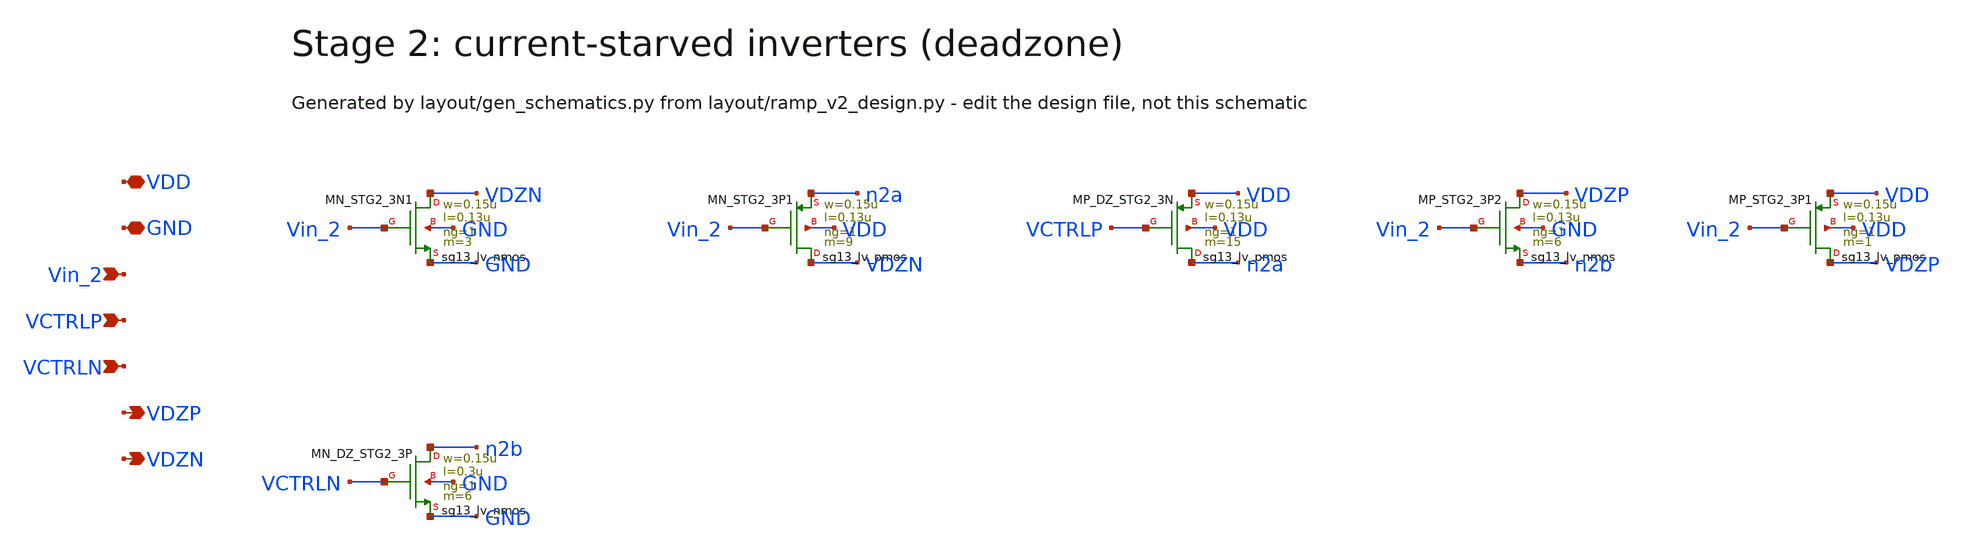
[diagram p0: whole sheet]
** sch_path: Design Files/RAMP/RAMP-V2/STG2_V2.sch
**.subckt STG2_V2 VDD GND Vin_2 VCTRLP VCTRLN VDZP VDZN
*.iopin VDD
*.iopin GND
*.ipin Vin_2
*.ipin VCTRLP
*.ipin VCTRLN
*.opin VDZP
*.opin VDZN
XMN_STG2_3N1 VDZN Vin_2 GND GND sg13_lv_nmos w=0.15u l=0.13u ng=1 m=3 mm_ok=1
XMN_STG2_3P1 VDZN Vin_2 n2a VDD sg13_lv_pmos w=0.15u l=0.13u ng=1 m=9 mm_ok=1
XMP_DZ_STG2_3N n2a VCTRLP VDD VDD sg13_lv_pmos w=0.15u l=0.13u ng=1 m=15 mm_ok=1
XMP_STG2_3P2 VDZP Vin_2 n2b GND sg13_lv_nmos w=0.15u l=0.13u ng=1 m=6 mm_ok=1
XMP_STG2_3P1 VDZP Vin_2 VDD VDD sg13_lv_pmos w=0.15u l=0.13u ng=1 m=1 mm_ok=1
XMN_DZ_STG2_3P n2b VCTRLN GND GND sg13_lv_nmos w=0.15u l=0.3u ng=1 m=6 mm_ok=1
**.ends
.end
